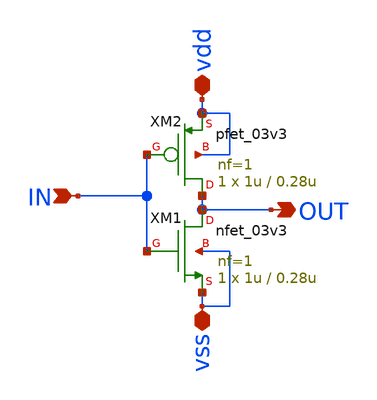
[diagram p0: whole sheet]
** sch_path: schematics/PC/INV/inv_pc.sch
**.subckt inv_pc IN OUT vdd vss
*.ipin IN
*.opin OUT
*.iopin vdd
*.iopin vss
XM1 OUT IN vss vss nfet_03v3 L=0.28u W=1u nf=1 ad='int((nf+1)/2) * W/nf * 0.18u' as='int((nf+2)/2) * W/nf * 0.18u'
+ pd='2*int((nf+1)/2) * (W/nf + 0.18u)' ps='2*int((nf+2)/2) * (W/nf + 0.18u)' nrd='0.18u / W' nrs='0.18u / W'
+ sa=0 sb=0 sd=0 m=1
XM2 OUT IN vdd vdd pfet_03v3 L=0.28u W=1u nf=1 ad='int((nf+1)/2) * W/nf * 0.18u' as='int((nf+2)/2) * W/nf * 0.18u'
+ pd='2*int((nf+1)/2) * (W/nf + 0.18u)' ps='2*int((nf+2)/2) * (W/nf + 0.18u)' nrd='0.18u / W' nrs='0.18u / W'
+ sa=0 sb=0 sd=0 m=1
**.ends
.end
